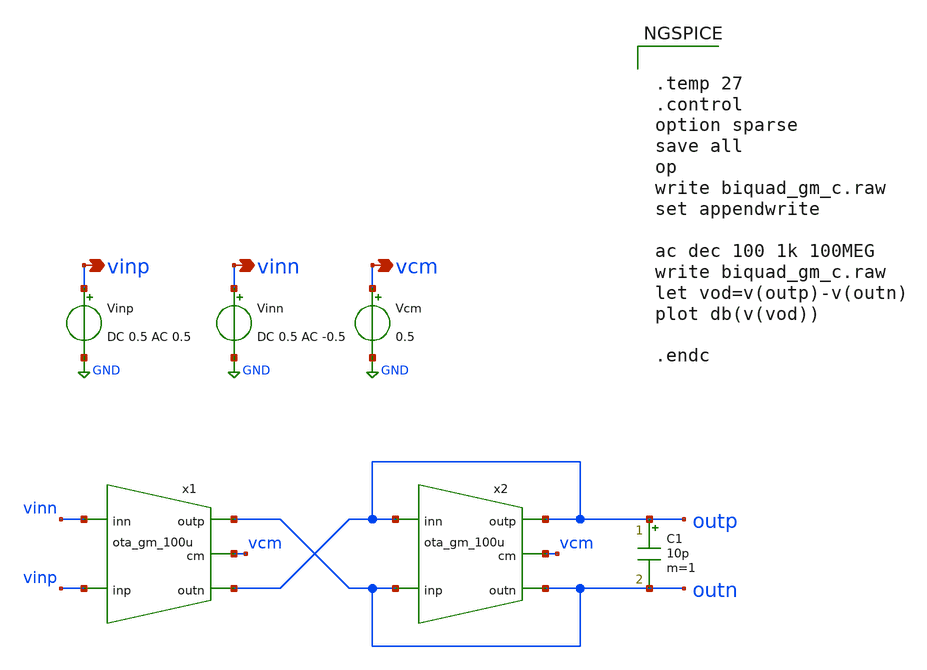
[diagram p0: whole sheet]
** sch_path: prj/template/2_Idealized_circuits/1st_ord_lp_gm_c.sch
**.subckt 1st_ord_lp_gm_c vinp vinn vcm
*.opin vinp
*.opin vinn
*.opin vcm
x1 vinp vinn outn outp vcm ota_gm_100u
x2 outn outp outp outn vcm ota_gm_100u
C1 outp outn 10p m=1
Vinp vinp GND DC 0.5 AC 0.5
Vinn vinn GND DC 0.5 AC -0.5
Vcm vcm GND 0.5
**** begin user architecture code


.temp 27
.control
option sparse
save all
op
write biquad_gm_c.raw
set appendwrite

ac dec 100 1k 100MEG
write biquad_gm_c.raw
let vod=v(outp)-v(outn)
plot db(v(vod))

.endc


**** end user architecture code
**.ends
.GLOBAL GND
.end
